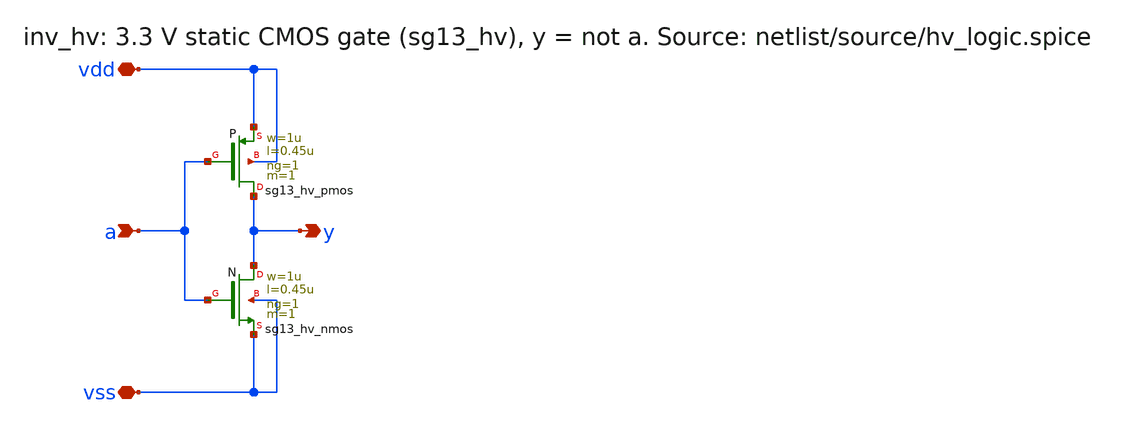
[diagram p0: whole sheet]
** sch_path: sudelbuecher/design_considerations/consolidation/bias_hierarchy_2026-10-27/before/macros/hv_logic/schematic/xschem/inv_hv.sch
**.subckt inv_hv vdd vss a y
*.iopin vdd
*.iopin vss
*.ipin a
*.opin y
XP y a vdd vdd sg13_hv_pmos w=1u l=0.45u ng=1 m=1 mm_ok=1
XN y a vss vss sg13_hv_nmos w=1u l=0.45u ng=1 m=1 mm_ok=1
**.ends
.end
